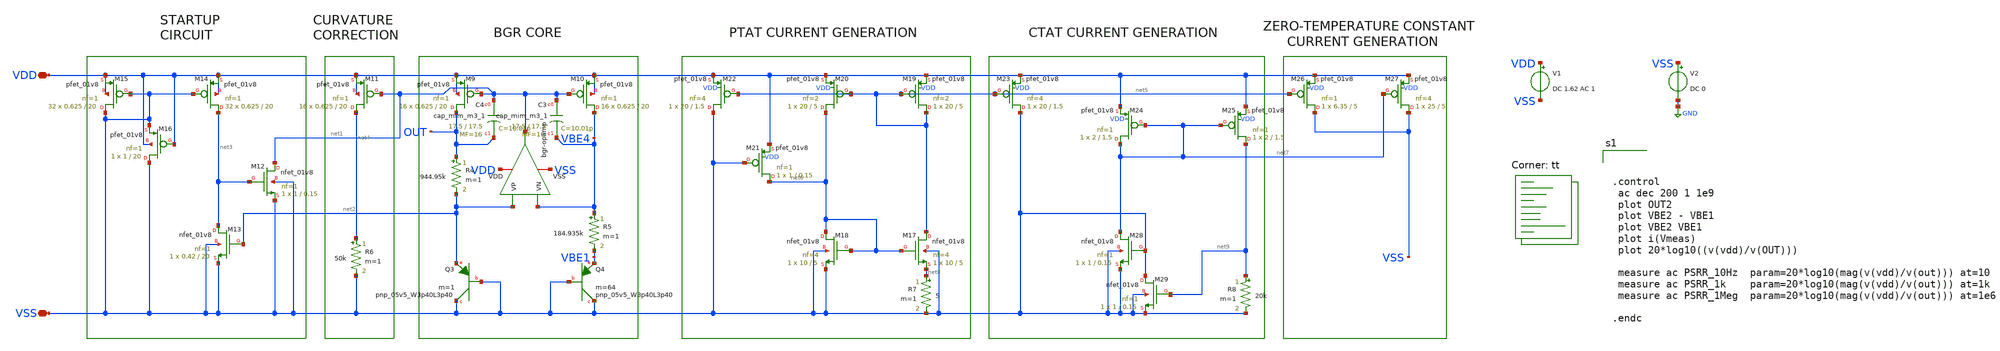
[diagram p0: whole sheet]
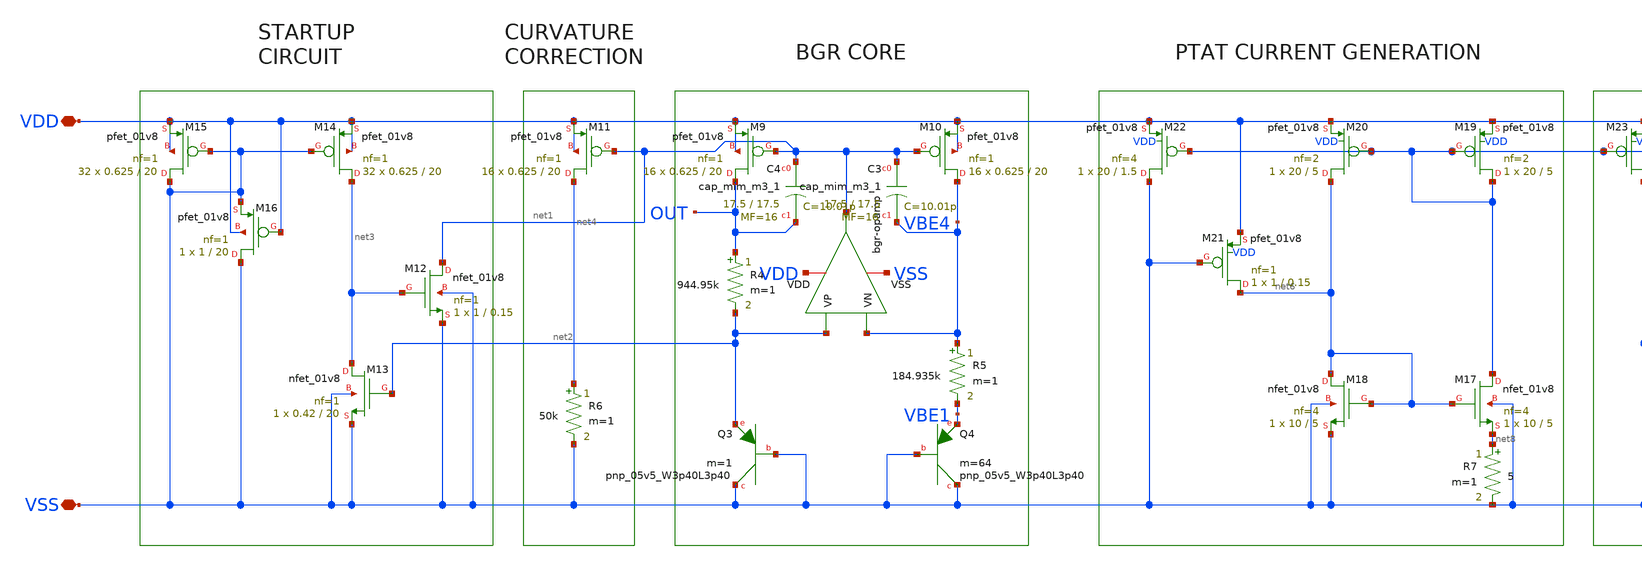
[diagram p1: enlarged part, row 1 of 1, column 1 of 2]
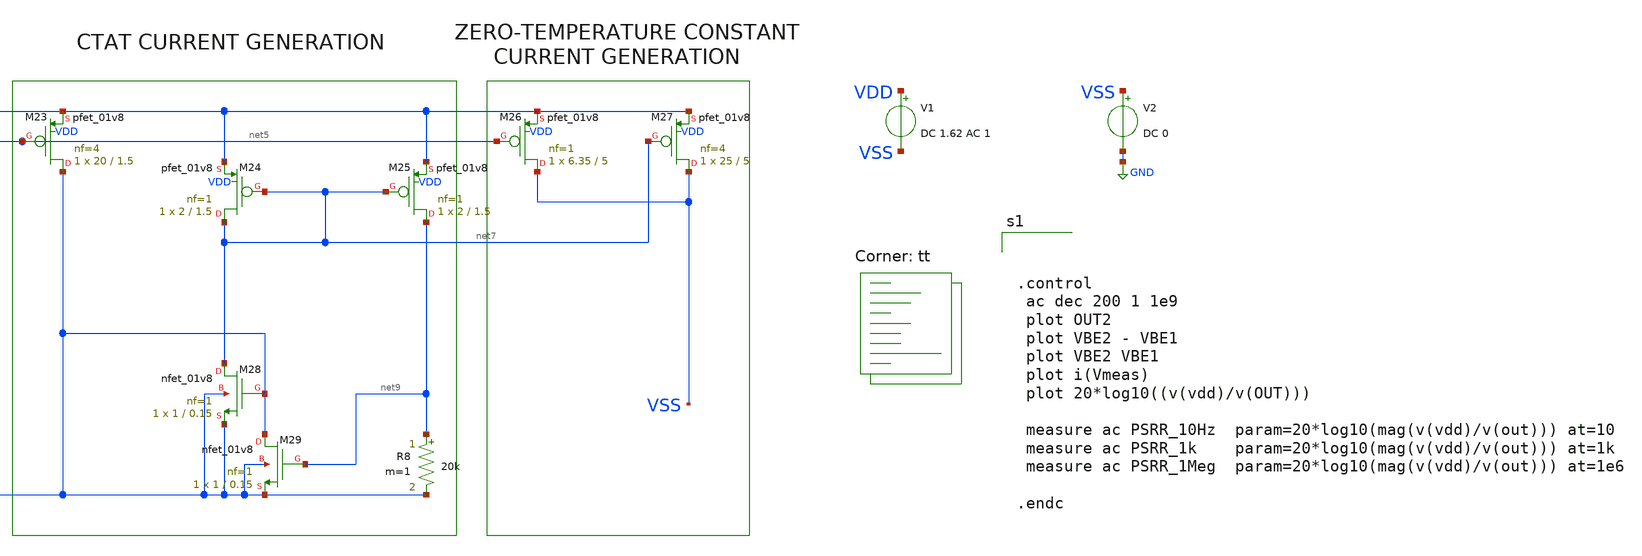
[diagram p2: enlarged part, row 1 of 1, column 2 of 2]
** sch_path: bandgap/bgr2-ac.sch
**.subckt bgr2-ac VDD VSS
*.iopin VDD
*.iopin VSS
V1 VDD VSS DC 1.62 AC 1
V2 VSS GND DC 0
x2 VDD net1 net2 VBE4 VSS bgr-opamp
XM9 OUT net1 VDD VDD sky130_fd_pr__pfet_01v8 L=20 W=0.625 nf=1 ad='int((nf+1)/2) * W/nf * 0.29' as='int((nf+2)/2) * W/nf * 0.29'
+ pd='2*int((nf+1)/2) * (W/nf + 0.29)' ps='2*int((nf+2)/2) * (W/nf + 0.29)' nrd='0.29 / W' nrs='0.29 / W'
+ sa=0 sb=0 sd=0 mult=16 m=16
XM10 VBE4 net1 VDD VDD sky130_fd_pr__pfet_01v8 L=20 W=0.625 nf=1 ad='int((nf+1)/2) * W/nf * 0.29' as='int((nf+2)/2) * W/nf * 0.29'
+ pd='2*int((nf+1)/2) * (W/nf + 0.29)' ps='2*int((nf+2)/2) * (W/nf + 0.29)' nrd='0.29 / W' nrs='0.29 / W'
+ sa=0 sb=0 sd=0 mult=16 m=16
R4 OUT net2 944.95k m=1
R5 VBE4 VBE1 184.935k m=1
XQ3 VSS VSS net2 sky130_fd_pr__pnp_05v5_W3p40L3p40 m=1
XQ4 VSS VSS VBE1 sky130_fd_pr__pnp_05v5_W3p40L3p40 m=64
XM11 net4 net1 VDD VDD sky130_fd_pr__pfet_01v8 L=20 W=0.625 nf=1 ad='int((nf+1)/2) * W/nf * 0.29' as='int((nf+2)/2) * W/nf * 0.29'
+ pd='2*int((nf+1)/2) * (W/nf + 0.29)' ps='2*int((nf+2)/2) * (W/nf + 0.29)' nrd='0.29 / W' nrs='0.29 / W'
+ sa=0 sb=0 sd=0 mult=16 m=16
XM12 net1 net3 VSS VSS sky130_fd_pr__nfet_01v8 L=0.15 W=1 nf=1 ad='int((nf+1)/2) * W/nf * 0.29' as='int((nf+2)/2) * W/nf * 0.29'
+ pd='2*int((nf+1)/2) * (W/nf + 0.29)' ps='2*int((nf+2)/2) * (W/nf + 0.29)' nrd='0.29 / W' nrs='0.29 / W'
+ sa=0 sb=0 sd=0 mult=1 m=1
XM13 net3 net2 VSS VSS sky130_fd_pr__nfet_01v8 L=20 W=0.42 nf=1 ad='int((nf+1)/2) * W/nf * 0.29' as='int((nf+2)/2) * W/nf * 0.29'
+ pd='2*int((nf+1)/2) * (W/nf + 0.29)' ps='2*int((nf+2)/2) * (W/nf + 0.29)' nrd='0.29 / W' nrs='0.29 / W'
+ sa=0 sb=0 sd=0 mult=1 m=1
XM14 net3 VSS VDD VDD sky130_fd_pr__pfet_01v8 L=20 W=0.625 nf=1 ad='int((nf+1)/2) * W/nf * 0.29' as='int((nf+2)/2) * W/nf * 0.29'
+ pd='2*int((nf+1)/2) * (W/nf + 0.29)' ps='2*int((nf+2)/2) * (W/nf + 0.29)' nrd='0.29 / W' nrs='0.29 / W'
+ sa=0 sb=0 sd=0 mult=32 m=32
XM15 VSS VSS VDD VDD sky130_fd_pr__pfet_01v8 L=20 W=0.625 nf=1 ad='int((nf+1)/2) * W/nf * 0.29' as='int((nf+2)/2) * W/nf * 0.29'
+ pd='2*int((nf+1)/2) * (W/nf + 0.29)' ps='2*int((nf+2)/2) * (W/nf + 0.29)' nrd='0.29 / W' nrs='0.29 / W'
+ sa=0 sb=0 sd=0 mult=32 m=32
XM16 VSS VDD VSS VDD sky130_fd_pr__pfet_01v8 L=20 W=1 nf=1 ad='int((nf+1)/2) * W/nf * 0.29' as='int((nf+2)/2) * W/nf * 0.29'
+ pd='2*int((nf+1)/2) * (W/nf + 0.29)' ps='2*int((nf+2)/2) * (W/nf + 0.29)' nrd='0.29 / W' nrs='0.29 / W'
+ sa=0 sb=0 sd=0 mult=1 m=1
R6 net4 VSS 50k m=1
XC3 net1 VBE4 sky130_fd_pr__cap_mim_m3_1 W=17.5 L=17.5 MF=16 m=16
XC4 net1 OUT sky130_fd_pr__cap_mim_m3_1 W=17.5 L=17.5 MF=16 m=16
XM17 net5 net6 net8 VSS sky130_fd_pr__nfet_01v8 L=5 W=10 nf=4 ad='int((nf+1)/2) * W/nf * 0.29' as='int((nf+2)/2) * W/nf * 0.29'
+ pd='2*int((nf+1)/2) * (W/nf + 0.29)' ps='2*int((nf+2)/2) * (W/nf + 0.29)' nrd='0.29 / W' nrs='0.29 / W'
+ sa=0 sb=0 sd=0 mult=1 m=1
XM18 net6 net6 VSS VSS sky130_fd_pr__nfet_01v8 L=5 W=10 nf=4 ad='int((nf+1)/2) * W/nf * 0.29' as='int((nf+2)/2) * W/nf * 0.29'
+ pd='2*int((nf+1)/2) * (W/nf + 0.29)' ps='2*int((nf+2)/2) * (W/nf + 0.29)' nrd='0.29 / W' nrs='0.29 / W'
+ sa=0 sb=0 sd=0 mult=1 m=1
XM19 net5 net5 VDD VDD sky130_fd_pr__pfet_01v8 L=5 W=20 nf=2 ad='int((nf+1)/2) * W/nf * 0.29' as='int((nf+2)/2) * W/nf * 0.29'
+ pd='2*int((nf+1)/2) * (W/nf + 0.29)' ps='2*int((nf+2)/2) * (W/nf + 0.29)' nrd='0.29 / W' nrs='0.29 / W'
+ sa=0 sb=0 sd=0 mult=1 m=1
XM20 net6 net5 VDD VDD sky130_fd_pr__pfet_01v8 L=5 W=20 nf=2 ad='int((nf+1)/2) * W/nf * 0.29' as='int((nf+2)/2) * W/nf * 0.29'
+ pd='2*int((nf+1)/2) * (W/nf + 0.29)' ps='2*int((nf+2)/2) * (W/nf + 0.29)' nrd='0.29 / W' nrs='0.29 / W'
+ sa=0 sb=0 sd=0 mult=1 m=1
XM21 net6 VSS VDD VDD sky130_fd_pr__pfet_01v8 L=0.15 W=1 nf=1 ad='int((nf+1)/2) * W/nf * 0.29' as='int((nf+2)/2) * W/nf * 0.29'
+ pd='2*int((nf+1)/2) * (W/nf + 0.29)' ps='2*int((nf+2)/2) * (W/nf + 0.29)' nrd='0.29 / W' nrs='0.29 / W'
+ sa=0 sb=0 sd=0 mult=1 m=1
XM22 VSS net5 VDD VDD sky130_fd_pr__pfet_01v8 L=1.5 W=20 nf=4 ad='int((nf+1)/2) * W/nf * 0.29' as='int((nf+2)/2) * W/nf * 0.29'
+ pd='2*int((nf+1)/2) * (W/nf + 0.29)' ps='2*int((nf+2)/2) * (W/nf + 0.29)' nrd='0.29 / W' nrs='0.29 / W'
+ sa=0 sb=0 sd=0 mult=1 m=1
XM23 VSS net5 VDD VDD sky130_fd_pr__pfet_01v8 L=1.5 W=20 nf=4 ad='int((nf+1)/2) * W/nf * 0.29' as='int((nf+2)/2) * W/nf * 0.29'
+ pd='2*int((nf+1)/2) * (W/nf + 0.29)' ps='2*int((nf+2)/2) * (W/nf + 0.29)' nrd='0.29 / W' nrs='0.29 / W'
+ sa=0 sb=0 sd=0 mult=1 m=1
XM24 net7 net7 VDD VDD sky130_fd_pr__pfet_01v8 L=1.5 W=2 nf=1 ad='int((nf+1)/2) * W/nf * 0.29' as='int((nf+2)/2) * W/nf * 0.29'
+ pd='2*int((nf+1)/2) * (W/nf + 0.29)' ps='2*int((nf+2)/2) * (W/nf + 0.29)' nrd='0.29 / W' nrs='0.29 / W'
+ sa=0 sb=0 sd=0 mult=1 m=1
XM25 net9 net7 VDD VDD sky130_fd_pr__pfet_01v8 L=1.5 W=2 nf=1 ad='int((nf+1)/2) * W/nf * 0.29' as='int((nf+2)/2) * W/nf * 0.29'
+ pd='2*int((nf+1)/2) * (W/nf + 0.29)' ps='2*int((nf+2)/2) * (W/nf + 0.29)' nrd='0.29 / W' nrs='0.29 / W'
+ sa=0 sb=0 sd=0 mult=1 m=1
XM26 VSS net5 VDD VDD sky130_fd_pr__pfet_01v8 L=5 W=6.35 nf=1 ad='int((nf+1)/2) * W/nf * 0.29' as='int((nf+2)/2) * W/nf * 0.29'
+ pd='2*int((nf+1)/2) * (W/nf + 0.29)' ps='2*int((nf+2)/2) * (W/nf + 0.29)' nrd='0.29 / W' nrs='0.29 / W'
+ sa=0 sb=0 sd=0 mult=1 m=1
XM27 VSS net7 VDD VDD sky130_fd_pr__pfet_01v8 L=5 W=25 nf=4 ad='int((nf+1)/2) * W/nf * 0.29' as='int((nf+2)/2) * W/nf * 0.29'
+ pd='2*int((nf+1)/2) * (W/nf + 0.29)' ps='2*int((nf+2)/2) * (W/nf + 0.29)' nrd='0.29 / W' nrs='0.29 / W'
+ sa=0 sb=0 sd=0 mult=1 m=1
XM28 net7 VSS VSS VSS sky130_fd_pr__nfet_01v8 L=0.15 W=1 nf=1 ad='int((nf+1)/2) * W/nf * 0.29' as='int((nf+2)/2) * W/nf * 0.29'
+ pd='2*int((nf+1)/2) * (W/nf + 0.29)' ps='2*int((nf+2)/2) * (W/nf + 0.29)' nrd='0.29 / W' nrs='0.29 / W'
+ sa=0 sb=0 sd=0 mult=1 m=1
XM29 VSS net9 VSS VSS sky130_fd_pr__nfet_01v8 L=0.15 W=1 nf=1 ad='int((nf+1)/2) * W/nf * 0.29' as='int((nf+2)/2) * W/nf * 0.29'
+ pd='2*int((nf+1)/2) * (W/nf + 0.29)' ps='2*int((nf+2)/2) * (W/nf + 0.29)' nrd='0.29 / W' nrs='0.29 / W'
+ sa=0 sb=0 sd=0 mult=1 m=1
R7 net8 VSS 5 m=1
R8 net9 VSS 20k m=1
**** begin user architecture code
.lib $::SKYWATER_MODELS/sky130.lib.spice tt



.control
 ac dec 200 1 1e9
 plot OUT2
 plot VBE2 - VBE1
 plot VBE2 VBE1
 plot i(Vmeas)
 plot 20*log10((v(vdd)/v(OUT)))

 measure ac PSRR_10Hz  param=20*log10(mag(v(vdd)/v(out))) at=10
 measure ac PSRR_1k    param=20*log10(mag(v(vdd)/v(out))) at=1k
 measure ac PSRR_1Meg  param=20*log10(mag(v(vdd)/v(out))) at=1e6

.endc


**** end user architecture code
**.ends

* expanding   symbol:  afe-icdec-teknofest-2026/bandgap/bgr-opamp/bgr-opamp.sym # of pins=5
** sym_path: bandgap/bgr-opamp/bgr-opamp.sym
** sch_path: bandgap/bgr-opamp/bgr-opamp.sch
.subckt bgr-opamp VDD OUT VP VN VSS
*.iopin VSS
*.iopin VDD
*.ipin VP
*.ipin VN
*.opin OUT
XM2 net2 VN net3 VSS sky130_fd_pr__nfet_01v8 L=0.3 W=30 nf=2 ad='int((nf+1)/2) * W/nf * 0.29' as='int((nf+2)/2) * W/nf * 0.29'
+ pd='2*int((nf+1)/2) * (W/nf + 0.29)' ps='2*int((nf+2)/2) * (W/nf + 0.29)' nrd='0.29 / W' nrs='0.29 / W'
+ sa=0 sb=0 sd=0 mult=1 m=1
XM4 net2 net1 VDD VDD sky130_fd_pr__pfet_01v8 L=1.25 W=10.8 nf=4 ad='int((nf+1)/2) * W/nf * 0.29' as='int((nf+2)/2) * W/nf * 0.29'
+ pd='2*int((nf+1)/2) * (W/nf + 0.29)' ps='2*int((nf+2)/2) * (W/nf + 0.29)' nrd='0.29 / W' nrs='0.29 / W'
+ sa=0 sb=0 sd=0 mult=1 m=1
XM3 net1 net1 VDD VDD sky130_fd_pr__pfet_01v8 L=1.25 W=10.8 nf=4 ad='int((nf+1)/2) * W/nf * 0.29' as='int((nf+2)/2) * W/nf * 0.29'
+ pd='2*int((nf+1)/2) * (W/nf + 0.29)' ps='2*int((nf+2)/2) * (W/nf + 0.29)' nrd='0.29 / W' nrs='0.29 / W'
+ sa=0 sb=0 sd=0 mult=1 m=1
XM5 net3 net11 VSS VSS sky130_fd_pr__nfet_01v8 L=1.25 W=3.4 nf=1 ad='int((nf+1)/2) * W/nf * 0.29' as='int((nf+2)/2) * W/nf * 0.29'
+ pd='2*int((nf+1)/2) * (W/nf + 0.29)' ps='2*int((nf+2)/2) * (W/nf + 0.29)' nrd='0.29 / W' nrs='0.29 / W'
+ sa=0 sb=0 sd=0 mult=1 m=1
XM9 net4 net5 net12 VSS sky130_fd_pr__nfet_01v8 L=1.25 W=13.6 nf=1 ad='int((nf+1)/2) * W/nf * 0.29' as='int((nf+2)/2) * W/nf * 0.29'
+ pd='2*int((nf+1)/2) * (W/nf + 0.29)' ps='2*int((nf+2)/2) * (W/nf + 0.29)' nrd='0.29 / W' nrs='0.29 / W'
+ sa=0 sb=0 sd=0 mult=1 m=1
XM8 net4 net4 VDD VDD sky130_fd_pr__pfet_01v8 L=1.25 W=10.8 nf=4 ad='int((nf+1)/2) * W/nf * 0.29' as='int((nf+2)/2) * W/nf * 0.29'
+ pd='2*int((nf+1)/2) * (W/nf + 0.29)' ps='2*int((nf+2)/2) * (W/nf + 0.29)' nrd='0.29 / W' nrs='0.29 / W'
+ sa=0 sb=0 sd=0 mult=1 m=1
XM11 net5 net4 VDD VDD sky130_fd_pr__pfet_01v8 L=1.25 W=10.8 nf=4 ad='int((nf+1)/2) * W/nf * 0.29' as='int((nf+2)/2) * W/nf * 0.29'
+ pd='2*int((nf+1)/2) * (W/nf + 0.29)' ps='2*int((nf+2)/2) * (W/nf + 0.29)' nrd='0.29 / W' nrs='0.29 / W'
+ sa=0 sb=0 sd=0 mult=1 m=1
XM10 net5 net5 net6 net6 sky130_fd_pr__nfet_01v8 L=1.25 W=3.4 nf=1 ad='int((nf+1)/2) * W/nf * 0.29' as='int((nf+2)/2) * W/nf * 0.29'
+ pd='2*int((nf+1)/2) * (W/nf + 0.29)' ps='2*int((nf+2)/2) * (W/nf + 0.29)' nrd='0.29 / W' nrs='0.29 / W'
+ sa=0 sb=0 sd=0 mult=1 m=1
XM6 OUT net2 VDD VDD sky130_fd_pr__pfet_01v8 L=1.25 W=100 nf=32 ad='int((nf+1)/2) * W/nf * 0.29' as='int((nf+2)/2) * W/nf * 0.29'
+ pd='2*int((nf+1)/2) * (W/nf + 0.29)' ps='2*int((nf+2)/2) * (W/nf + 0.29)' nrd='0.29 / W' nrs='0.29 / W'
+ sa=0 sb=0 sd=0 mult=1 m=1
XM7 OUT net11 VSS VSS sky130_fd_pr__nfet_01v8 L=1.25 W=14 nf=4 ad='int((nf+1)/2) * W/nf * 0.29' as='int((nf+2)/2) * W/nf * 0.29'
+ pd='2*int((nf+1)/2) * (W/nf + 0.29)' ps='2*int((nf+2)/2) * (W/nf + 0.29)' nrd='0.29 / W' nrs='0.29 / W'
+ sa=0 sb=0 sd=0 mult=1 m=1
XC2 OUT net2 sky130_fd_pr__cap_mim_m3_1 W=25 L=25 MF=32 m=32
XR2 net7 net12 VSS sky130_fd_pr__res_high_po_1p41 L=3.235 mult=1 m=1
XR3 net9 net7 VSS sky130_fd_pr__res_high_po_1p41 L=3.235 mult=1 m=1
XR4 net8 net9 VSS sky130_fd_pr__res_high_po_1p41 L=3.235 mult=1 m=1
XR5 net10 net8 VSS sky130_fd_pr__res_high_po_1p41 L=3.235 mult=1 m=1
XR6 VSS net10 VSS sky130_fd_pr__res_high_po_1p41 L=3.235 mult=1 m=1
XM13 net11 net4 VDD VDD sky130_fd_pr__pfet_01v8 L=1.25 W=10.8 nf=4 ad='int((nf+1)/2) * W/nf * 0.29' as='int((nf+2)/2) * W/nf * 0.29'
+ pd='2*int((nf+1)/2) * (W/nf + 0.29)' ps='2*int((nf+2)/2) * (W/nf + 0.29)' nrd='0.29 / W' nrs='0.29 / W'
+ sa=0 sb=0 sd=0 mult=1 m=1
XM14 net11 net11 VSS VSS sky130_fd_pr__nfet_01v8 L=1.25 W=6.8 nf=1 ad='int((nf+1)/2) * W/nf * 0.29' as='int((nf+2)/2) * W/nf * 0.29'
+ pd='2*int((nf+1)/2) * (W/nf + 0.29)' ps='2*int((nf+2)/2) * (W/nf + 0.29)' nrd='0.29 / W' nrs='0.29 / W'
+ sa=0 sb=0 sd=0 mult=1 m=1
XM15 net6 net6 VSS VSS sky130_fd_pr__nfet_01v8 L=1.25 W=3.4 nf=1 ad='int((nf+1)/2) * W/nf * 0.29' as='int((nf+2)/2) * W/nf * 0.29'
+ pd='2*int((nf+1)/2) * (W/nf + 0.29)' ps='2*int((nf+2)/2) * (W/nf + 0.29)' nrd='0.29 / W' nrs='0.29 / W'
+ sa=0 sb=0 sd=0 mult=1 m=1
XM12 net5 net4 net4 VSS sky130_fd_pr__pfet_01v8 L=0.15 W=0.85 nf=1 ad='int((nf+1)/2) * W/nf * 0.29' as='int((nf+2)/2) * W/nf * 0.29'
+ pd='2*int((nf+1)/2) * (W/nf + 0.29)' ps='2*int((nf+2)/2) * (W/nf + 0.29)' nrd='0.29 / W' nrs='0.29 / W'
+ sa=0 sb=0 sd=0 mult=1 m=1
XM16 net1 VP net3 VSS sky130_fd_pr__nfet_01v8 L=0.3 W=30 nf=2 ad='int((nf+1)/2) * W/nf * 0.29' as='int((nf+2)/2) * W/nf * 0.29'
+ pd='2*int((nf+1)/2) * (W/nf + 0.29)' ps='2*int((nf+2)/2) * (W/nf + 0.29)' nrd='0.29 / W' nrs='0.29 / W'
+ sa=0 sb=0 sd=0 mult=1 m=1
.ends

.GLOBAL GND
.end
